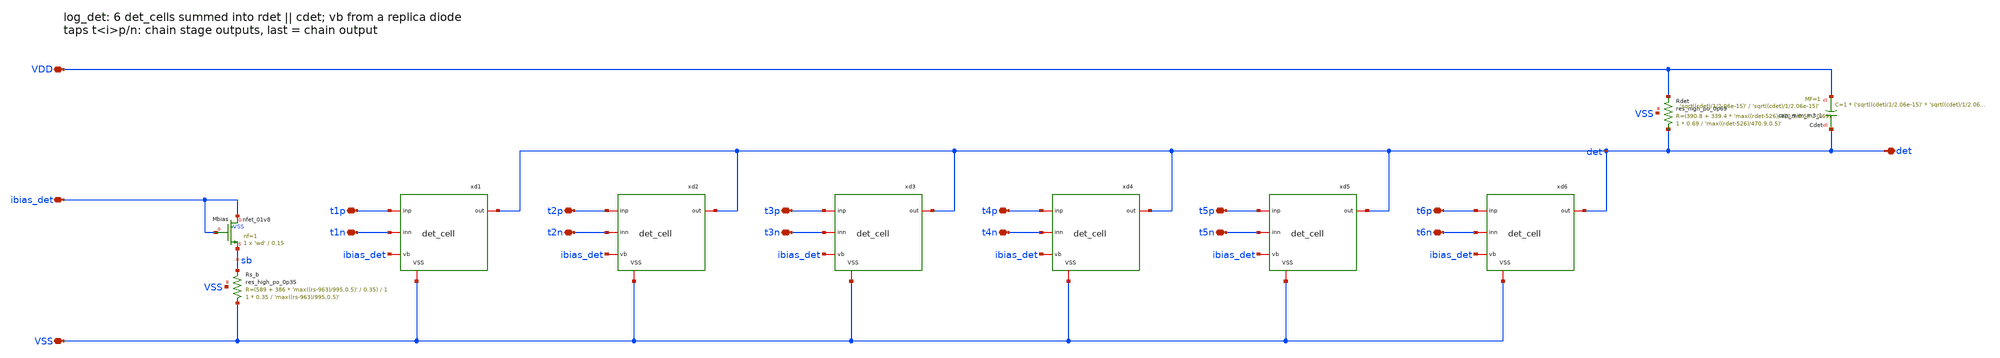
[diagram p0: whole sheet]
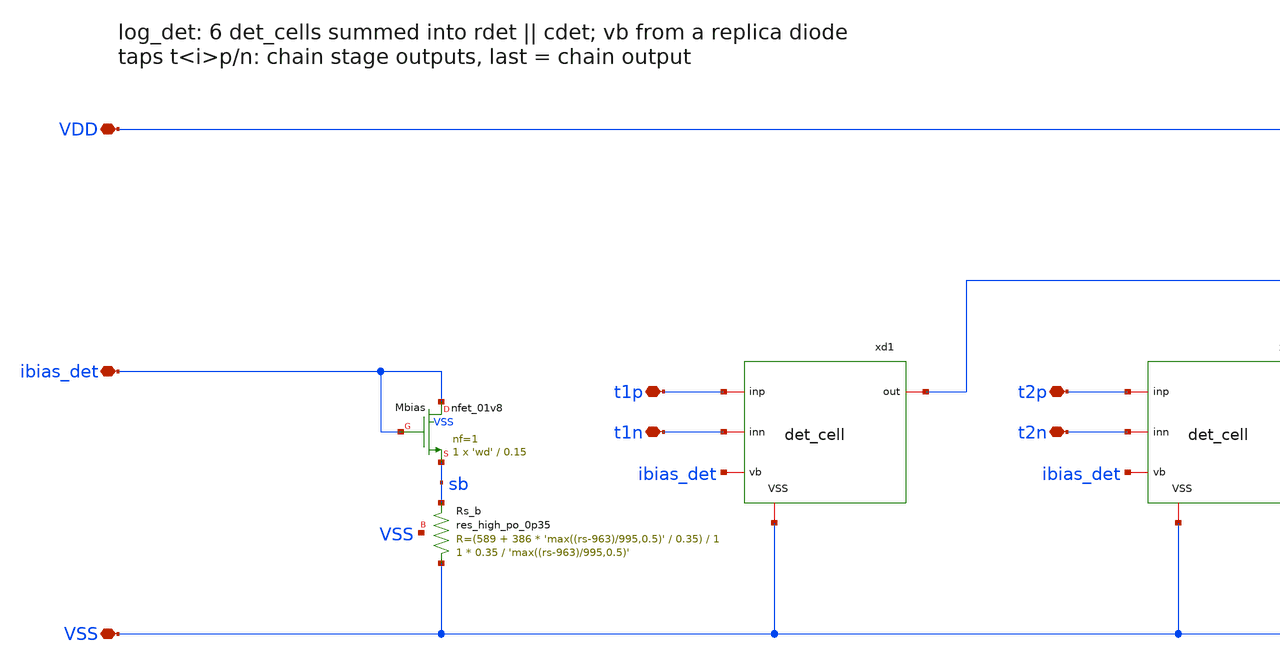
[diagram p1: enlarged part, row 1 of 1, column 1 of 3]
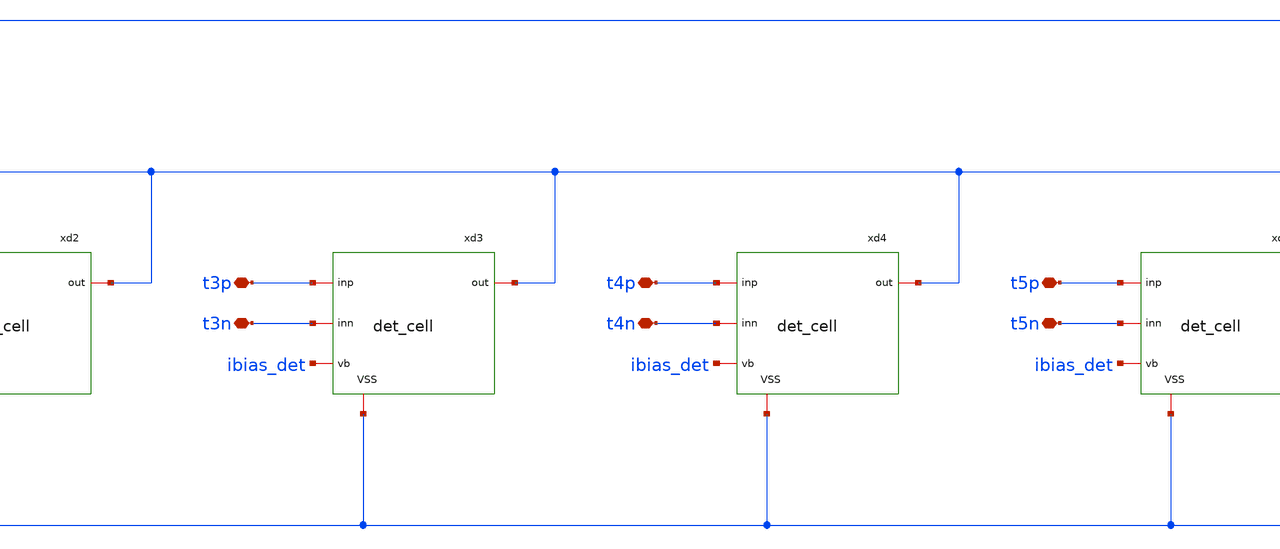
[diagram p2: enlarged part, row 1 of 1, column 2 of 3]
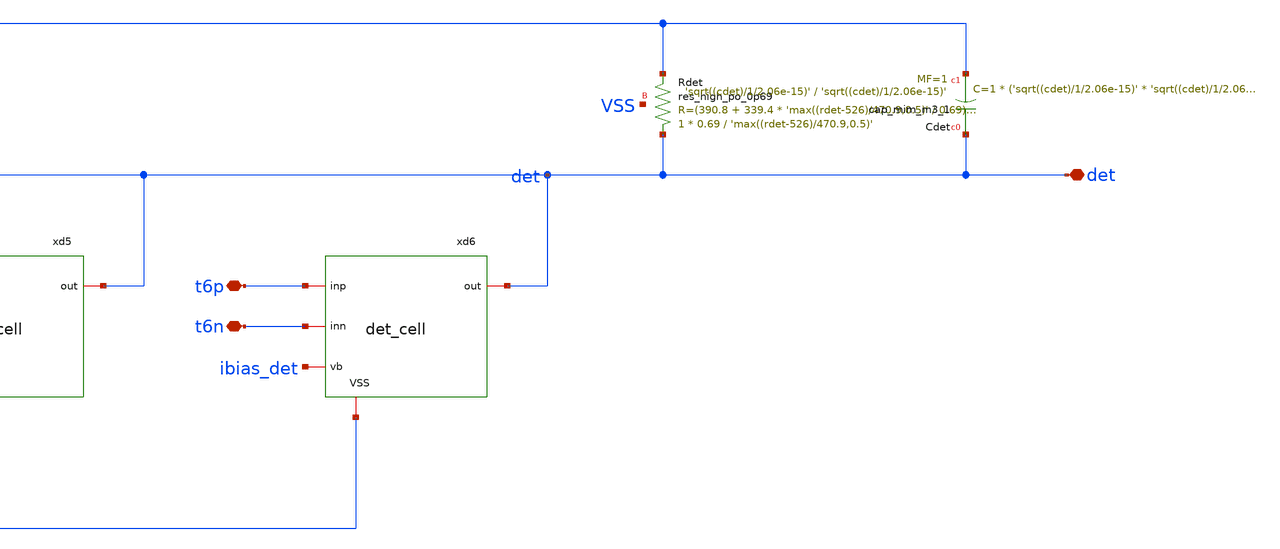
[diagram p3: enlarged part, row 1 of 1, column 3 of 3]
** sch_path: xschem/log_det.sch
**.subckt log_det VDD VSS ibias_det det t1p t1n t2p t2n t3p t3n t4p t4n t5p t5n t6p t6n
*.iopin VDD
*.iopin VSS
*.iopin ibias_det
*.iopin det
*.iopin t1p
*.iopin t1n
*.iopin t2p
*.iopin t2n
*.iopin t3p
*.iopin t3n
*.iopin t4p
*.iopin t4n
*.iopin t5p
*.iopin t5n
*.iopin t6p
*.iopin t6n
XMbias ibias_det ibias_det sb VSS sky130_fd_pr__nfet_01v8 L=0.15 W='wd' nf=1 ad='int((nf+1)/2) * W/nf * 0.29'
+ as='int((nf+2)/2) * W/nf * 0.29' pd='2*int((nf+1)/2) * (W/nf + 0.29)' ps='2*int((nf+2)/2) * (W/nf + 0.29)'
+ nrd='0.29 / W' nrs='0.29 / W' sa=0 sb=0 sd=0 mult=1 m=1
XRs_b VSS sb VSS sky130_fd_pr__res_high_po_0p35 L='max((rs-963)/995,0.5)' mult=1 m=1
XRdet det VDD VSS sky130_fd_pr__res_high_po_0p69 L='max((rdet-526)/470.9,0.5)' mult=1 m=1
XCdet det VDD sky130_fd_pr__cap_mim_m3_1 W='sqrt((cdet)/1/2.06e-15)' L='sqrt((cdet)/1/2.06e-15)' MF=1
+ m=1
xd1 t1p t1n ibias_det det VSS det_cell wd='wd' rs='rs' cc='cc' rb='rb'
xd2 t2p t2n ibias_det det VSS det_cell wd='wd' rs='rs' cc='cc' rb='rb'
xd3 t3p t3n ibias_det det VSS det_cell wd='wd' rs='rs' cc='cc' rb='rb'
xd4 t4p t4n ibias_det det VSS det_cell wd='wd' rs='rs' cc='cc' rb='rb'
xd5 t5p t5n ibias_det det VSS det_cell wd='wd' rs='rs' cc='cc' rb='rb'
xd6 t6p t6n ibias_det det VSS det_cell wd='wd' rs='rs' cc='cc' rb='rb'
**.ends

* expanding   symbol:  det_cell.sym # of pins=5
** sym_path: xschem/det_cell.sym
** sch_path: xschem/det_cell.sch
.subckt det_cell inp inn vb out VSS  wd=1 rs=10k cc=100f rb=200k
*.iopin VSS
*.iopin vb
*.iopin inp
*.iopin inn
*.iopin out
XCc_p gp inp sky130_fd_pr__cap_mim_m3_1 W='sqrt((cc)/1/2.06e-15)' L='sqrt((cc)/1/2.06e-15)' MF=1 m=1
XRb_p gp vb VSS sky130_fd_pr__res_xhigh_po_0p35 L='max((rb-0)/7379,0.5)' mult=1 m=1
XMp out gp sp VSS sky130_fd_pr__nfet_01v8 L=0.15 W='wd' nf=1 ad='int((nf+1)/2) * W/nf * 0.29' as='int((nf+2)/2) * W/nf * 0.29'
+ pd='2*int((nf+1)/2) * (W/nf + 0.29)' ps='2*int((nf+2)/2) * (W/nf + 0.29)' nrd='0.29 / W' nrs='0.29 / W'
+ sa=0 sb=0 sd=0 mult=1 m=1
XRs_p VSS sp VSS sky130_fd_pr__res_high_po_0p35 L='max((rs-963)/995,0.5)' mult=1 m=1
XCc_n gn inn sky130_fd_pr__cap_mim_m3_1 W='sqrt((cc)/1/2.06e-15)' L='sqrt((cc)/1/2.06e-15)' MF=1 m=1
XRb_n gn vb VSS sky130_fd_pr__res_xhigh_po_0p35 L='max((rb-0)/7379,0.5)' mult=1 m=1
XMn out gn sn VSS sky130_fd_pr__nfet_01v8 L=0.15 W='wd' nf=1 ad='int((nf+1)/2) * W/nf * 0.29' as='int((nf+2)/2) * W/nf * 0.29'
+ pd='2*int((nf+1)/2) * (W/nf + 0.29)' ps='2*int((nf+2)/2) * (W/nf + 0.29)' nrd='0.29 / W' nrs='0.29 / W'
+ sa=0 sb=0 sd=0 mult=1 m=1
XRs_n VSS sn VSS sky130_fd_pr__res_high_po_0p35 L='max((rs-963)/995,0.5)' mult=1 m=1
.ends

.end
